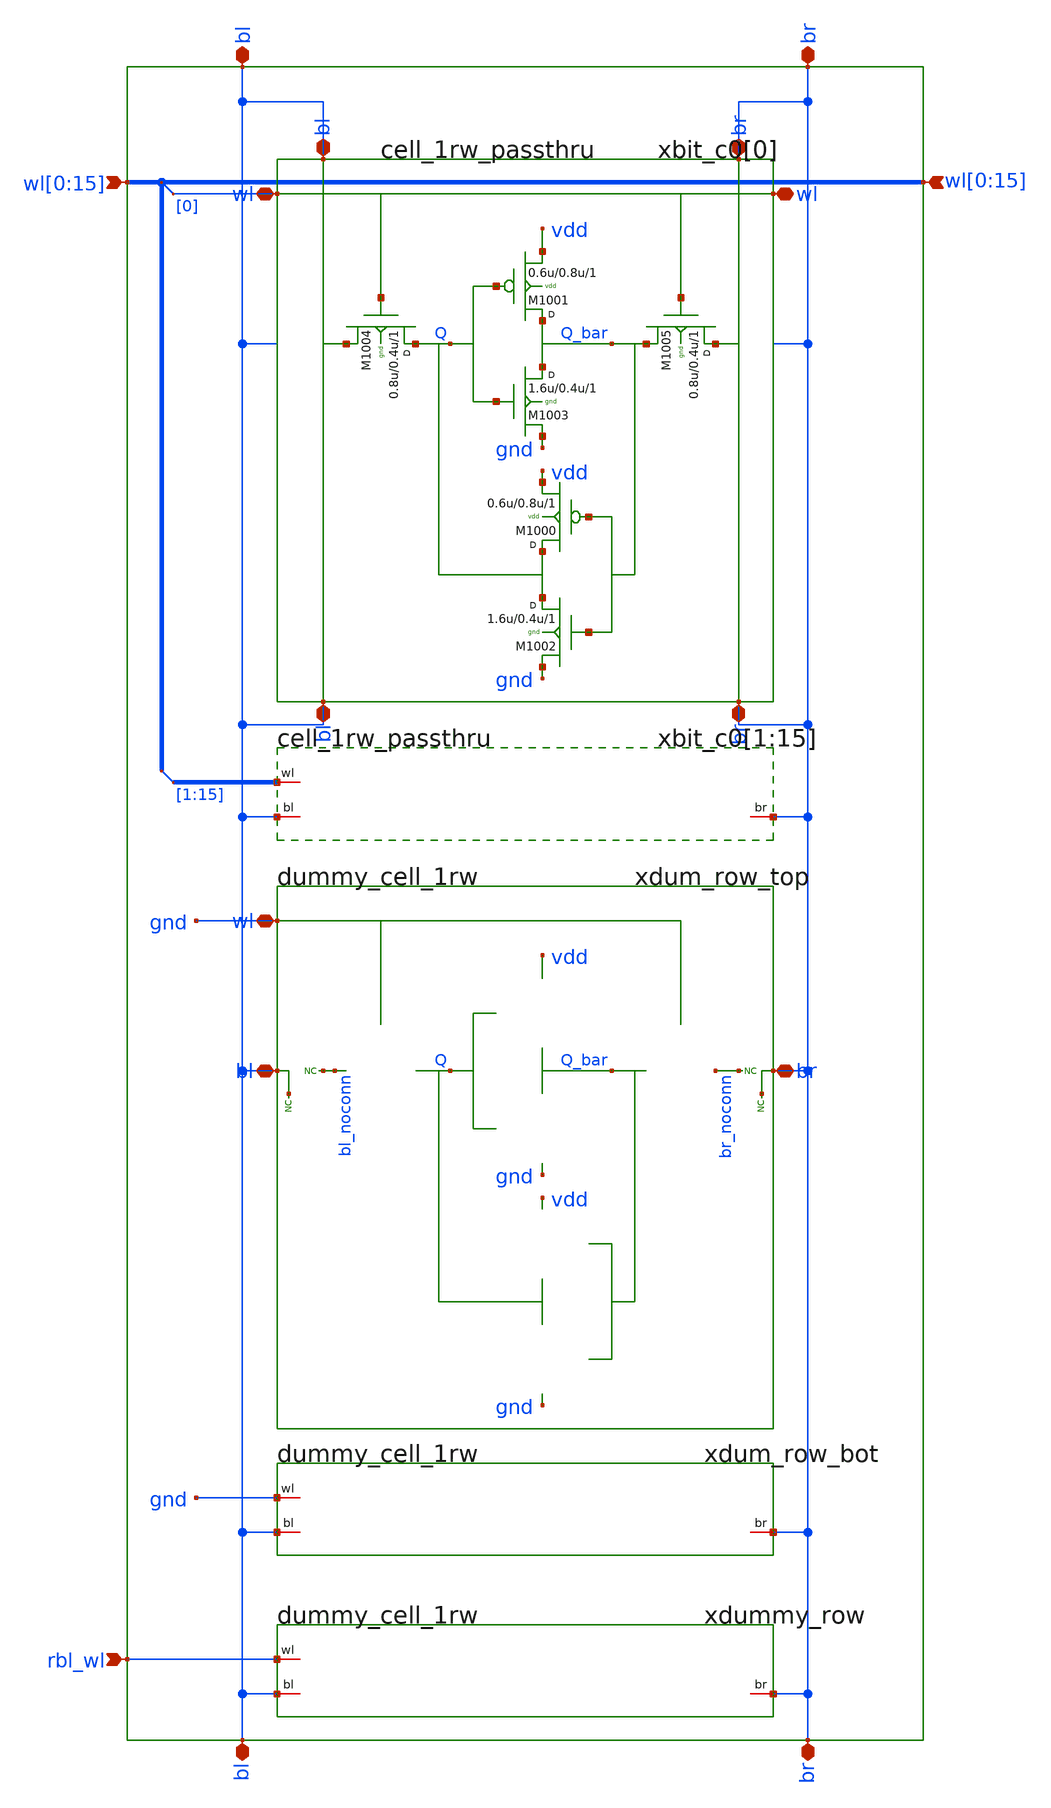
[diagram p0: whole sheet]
** sch_path: sram_2_64_scn4m_lcc/1column.sch
**.subckt 1column bl br rbl_wl
*+ wl[0],wl[1],wl[2],wl[3],wl[4],wl[5],wl[6],wl[7],wl[8],wl[9],wl[10],wl[11],wl[12],wl[13],wl[14],wl[15] bl br
*+ wl[0],wl[1],wl[2],wl[3],wl[4],wl[5],wl[6],wl[7],wl[8],wl[9],wl[10],wl[11],wl[12],wl[13],wl[14],wl[15]
*.iopin bl
*.iopin br
*.ipin rbl_wl
*.ipin
*+ wl[0],wl[1],wl[2],wl[3],wl[4],wl[5],wl[6],wl[7],wl[8],wl[9],wl[10],wl[11],wl[12],wl[13],wl[14],wl[15]
*.iopin bl
*.iopin br
*.ipin
*+ wl[0],wl[1],wl[2],wl[3],wl[4],wl[5],wl[6],wl[7],wl[8],wl[9],wl[10],wl[11],wl[12],wl[13],wl[14],wl[15]
xbit_c0[0] bl br wl[0] vdd gnd cell_1rw_passthru
xdum_row_top bl br gnd vdd gnd dummy_cell_1rw
xdum_row_bot bl br gnd vdd gnd dummy_cell_1rw
xdummy_row bl br rbl_wl vdd gnd dummy_cell_1rw
xbit_c0[1] bl br wl[1] vdd gnd cell_1rw_passthru
xbit_c0[2] bl br wl[2] vdd gnd cell_1rw_passthru
xbit_c0[3] bl br wl[3] vdd gnd cell_1rw_passthru
xbit_c0[4] bl br wl[4] vdd gnd cell_1rw_passthru
xbit_c0[5] bl br wl[5] vdd gnd cell_1rw_passthru
xbit_c0[6] bl br wl[6] vdd gnd cell_1rw_passthru
xbit_c0[7] bl br wl[7] vdd gnd cell_1rw_passthru
xbit_c0[8] bl br wl[8] vdd gnd cell_1rw_passthru
xbit_c0[9] bl br wl[9] vdd gnd cell_1rw_passthru
xbit_c0[10] bl br wl[10] vdd gnd cell_1rw_passthru
xbit_c0[11] bl br wl[11] vdd gnd cell_1rw_passthru
xbit_c0[12] bl br wl[12] vdd gnd cell_1rw_passthru
xbit_c0[13] bl br wl[13] vdd gnd cell_1rw_passthru
xbit_c0[14] bl br wl[14] vdd gnd cell_1rw_passthru
xbit_c0[15] bl br wl[15] vdd gnd cell_1rw_passthru
* tap: wl[0:15] --> wl[0]
* tap: wl[0:15] --> wl[1:15]
**.ends

* expanding   symbol:  cell_1rw_passthru.sch # of pins=6
** sym_path: sram_2_64_scn4m_lcc/cell_1rw_passthru.sch
** sch_path: sram_2_64_scn4m_lcc/cell_1rw_passthru.sch
.subckt cell_1rw_passthru bl br wl vdd gnd
*.iopin bl
*.iopin br
*.iopin wl
*.iopin wl
*.iopin bl
*.iopin br
M1003 Q_bar Q gnd gnd n w=1.6u l=0.4u m=1
M1004 Q wl bl gnd n w=0.8u l=0.4u m=1
M1001 Q_bar Q vdd vdd p w=0.6u l=0.8u m=1
M1005 br wl Q_bar gnd n w=0.8u l=0.4u m=1
M1002 Q Q_bar gnd gnd n w=1.6u l=0.4u m=1
M1000 Q Q_bar vdd vdd p w=0.6u l=0.8u m=1
.ends


* expanding   symbol:  dummy_cell_1rw.sch # of pins=3
** sym_path: sram_2_64_scn4m_lcc/dummy_cell_1rw.sch
** sch_path: sram_2_64_scn4m_lcc/dummy_cell_1rw.sch
.subckt dummy_cell_1rw bl br wl vdd gnd
*.iopin bl
*.iopin br
*.iopin wl
XM1004 Q wl bl_noconn gnd sky130_fd_pr__nfet_01v8 L=0.4 W=0.8 nf=1 ad='int((nf+1)/2) * W/nf * 0.29' as='int((nf+2)/2) * W/nf * 0.29'
+ pd='2*int((nf+1)/2) * (W/nf + 0.29)' ps='2*int((nf+2)/2) * (W/nf + 0.29)' nrd='0.29 / W' nrs='0.29 / W'
+ sa=0 sb=0 sd=0 mult=1 m=1
XM1001 Q_bar Q vdd vdd sky130_fd_pr__pfet_01v8 L=0.8 W=0.6 nf=1 ad='int((nf+1)/2) * W/nf * 0.29' as='int((nf+2)/2) * W/nf * 0.29'
+ pd='2*int((nf+1)/2) * (W/nf + 0.29)' ps='2*int((nf+2)/2) * (W/nf + 0.29)' nrd='0.29 / W' nrs='0.29 / W'
+ sa=0 sb=0 sd=0 mult=1 m=1
XM1003 Q_bar Q gnd gnd sky130_fd_pr__nfet_01v8 L=0.4 W=1.6 nf=1 ad='int((nf+1)/2) * W/nf * 0.29' as='int((nf+2)/2) * W/nf * 0.29'
+ pd='2*int((nf+1)/2) * (W/nf + 0.29)' ps='2*int((nf+2)/2) * (W/nf + 0.29)' nrd='0.29 / W' nrs='0.29 / W'
+ sa=0 sb=0 sd=0 mult=1 m=1
XM1002 Q Q_bar gnd gnd sky130_fd_pr__nfet_01v8 L=0.4 W=1.6 nf=1 ad='int((nf+1)/2) * W/nf * 0.29' as='int((nf+2)/2) * W/nf * 0.29'
+ pd='2*int((nf+1)/2) * (W/nf + 0.29)' ps='2*int((nf+2)/2) * (W/nf + 0.29)' nrd='0.29 / W' nrs='0.29 / W'
+ sa=0 sb=0 sd=0 mult=1 m=1
XM1000 Q Q_bar vdd vdd sky130_fd_pr__pfet_01v8 L=0.8 W=0.6 nf=1 ad='int((nf+1)/2) * W/nf * 0.29' as='int((nf+2)/2) * W/nf * 0.29'
+ pd='2*int((nf+1)/2) * (W/nf + 0.29)' ps='2*int((nf+2)/2) * (W/nf + 0.29)' nrd='0.29 / W' nrs='0.29 / W'
+ sa=0 sb=0 sd=0 mult=1 m=1
XM1005 br_noconn wl Q_bar gnd sky130_fd_pr__nfet_01v8 L=0.4 W=0.8 nf=1 ad='int((nf+1)/2) * W/nf * 0.29'
+ as='int((nf+2)/2) * W/nf * 0.29' pd='2*int((nf+1)/2) * (W/nf + 0.29)' ps='2*int((nf+2)/2) * (W/nf + 0.29)'
+ nrd='0.29 / W' nrs='0.29 / W' sa=0 sb=0 sd=0 mult=1 m=1
* noconn bl_noconn
* noconn br_noconn
* noconn br
* noconn bl
.ends

.end
